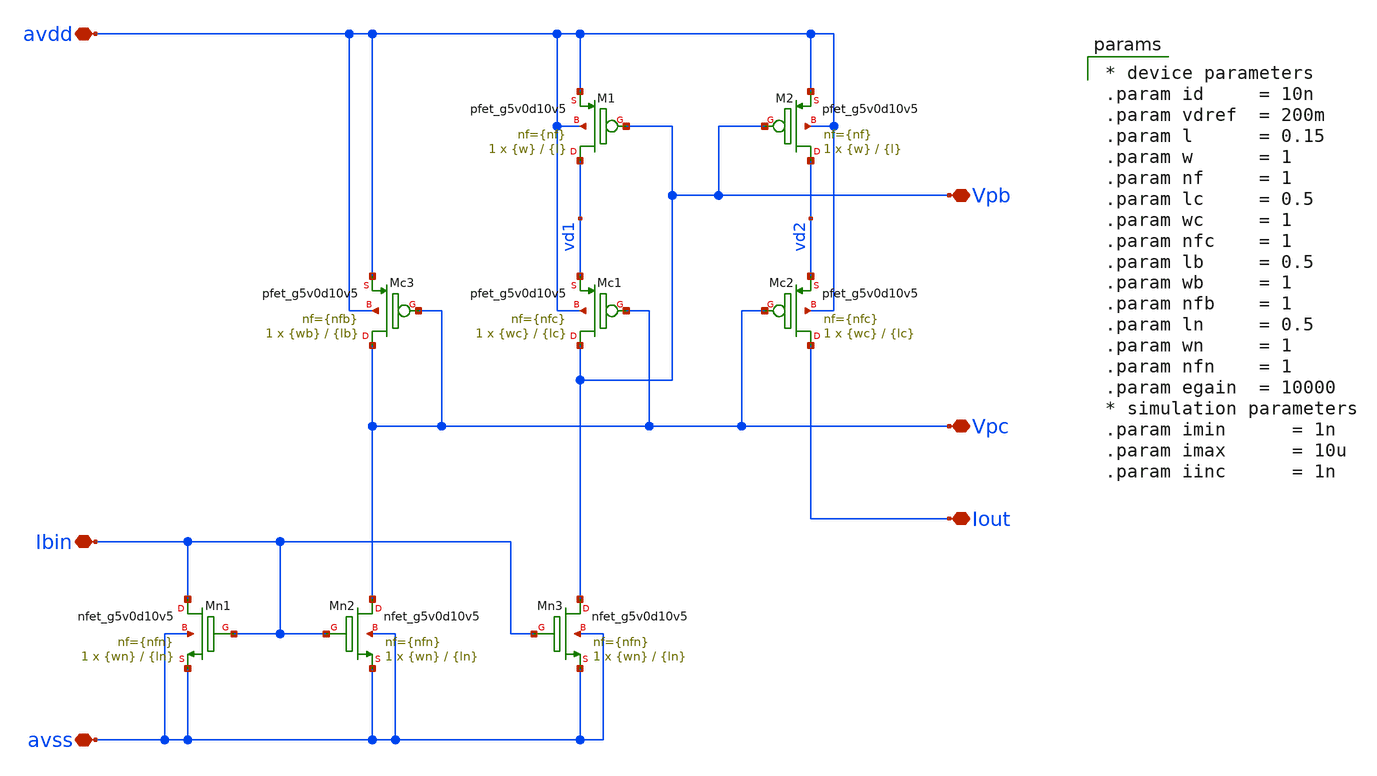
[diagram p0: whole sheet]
** sch_path: xschem/sky130_cm_ip__biasgen.sch
**.subckt sky130_cm_ip__biasgen avss avdd Ibin Vpb Vpc Iout
*.iopin avss
*.iopin avdd
*.iopin Ibin
*.iopin Vpb
*.iopin Vpc
*.iopin Iout
XMc1 Vpb Vpc vd1 avdd sky130_fd_pr__pfet_g5v0d10v5 L={lc} W={wc} nf={nfc} ad='int(({nfc} + 1)/2) * {wc} / {nfc} * 0.29'
+ as='int(({nfc} + 2)/2) * {wc} / {nfc} * 0.29' pd='2*int(({nfc} + 1)/2) * ({wc} / {nfc} + 0.29)' ps='2*int(({nfc} + 2)/2) * ({wc} / {nfc} + 0.29)'
+ nrd='0.29 / {wc} ' nrs='0.29 / {wc} ' sa=0 sb=0 sd=0 mult=1 m=1
XM1 vd1 Vpb avdd avdd sky130_fd_pr__pfet_g5v0d10v5 L={l} W={w} nf={nf} ad='int(({nf} + 1)/2) * {w} / {nf} * 0.29'
+ as='int(({nf} + 2)/2) * {w} / {nf} * 0.29' pd='2*int(({nf} + 1)/2) * ({w} / {nf} + 0.29)' ps='2*int(({nf} + 2)/2) * ({w} / {nf} + 0.29)'
+ nrd='0.29 / {w} ' nrs='0.29 / {w} ' sa=0 sb=0 sd=0 mult=1 m=1
XMc2 Iout Vpc vd2 avdd sky130_fd_pr__pfet_g5v0d10v5 L={lc} W={wc} nf={nfc} ad='int(({nfc} + 1)/2) * {wc} / {nfc} * 0.29'
+ as='int(({nfc} + 2)/2) * {wc} / {nfc} * 0.29' pd='2*int(({nfc} + 1)/2) * ({wc} / {nfc} + 0.29)' ps='2*int(({nfc} + 2)/2) * ({wc} / {nfc} + 0.29)'
+ nrd='0.29 / {wc} ' nrs='0.29 / {wc} ' sa=0 sb=0 sd=0 mult=1 m=1
XM2 vd2 Vpb avdd avdd sky130_fd_pr__pfet_g5v0d10v5 L={l} W={w} nf={nf} ad='int(({nf} + 1)/2) * {w} / {nf} * 0.29'
+ as='int(({nf} + 2)/2) * {w} / {nf} * 0.29' pd='2*int(({nf} + 1)/2) * ({w} / {nf} + 0.29)' ps='2*int(({nf} + 2)/2) * ({w} / {nf} + 0.29)'
+ nrd='0.29 / {w} ' nrs='0.29 / {w} ' sa=0 sb=0 sd=0 mult=1 m=1
XMc3 Vpc Vpc avdd avdd sky130_fd_pr__pfet_g5v0d10v5 L={lb} W={wb} nf={nfb} ad='int(({nfb} + 1)/2) * {wb} / {nfb} * 0.29'
+ as='int(({nfb} + 2)/2) * {wb} / {nfb} * 0.29' pd='2*int(({nfb} + 1)/2) * ({wb} / {nfb} + 0.29)' ps='2*int(({nfb} + 2)/2) * ({wb} / {nfb} + 0.29)'
+ nrd='0.29 / {wb} ' nrs='0.29 / {wb} ' sa=0 sb=0 sd=0 mult=1 m=1
XMn1 Ibin Ibin avss avss sky130_fd_pr__nfet_g5v0d10v5 L={ln} W={wn} nf={nfn} ad='int(({nfn} + 1)/2) * {wn} / {nfn} * 0.29'
+ as='int(({nfn} + 2)/2) * {wn} / {nfn} * 0.29' pd='2*int(({nfn} + 1)/2) * ({wn} / {nfn} + 0.29)' ps='2*int(({nfn} + 2)/2) * ({wn} / {nfn} + 0.29)'
+ nrd='0.29 / {wn} ' nrs='0.29 / {wn} ' sa=0 sb=0 sd=0 mult=1 m=1
XMn2 Vpc Ibin avss avss sky130_fd_pr__nfet_g5v0d10v5 L={ln} W={wn} nf={nfn} ad='int(({nfn} + 1)/2) * {wn} / {nfn} * 0.29'
+ as='int(({nfn} + 2)/2) * {wn} / {nfn} * 0.29' pd='2*int(({nfn} + 1)/2) * ({wn} / {nfn} + 0.29)' ps='2*int(({nfn} + 2)/2) * ({wn} / {nfn} + 0.29)'
+ nrd='0.29 / {wn} ' nrs='0.29 / {wn} ' sa=0 sb=0 sd=0 mult=1 m=1
XMn3 Vpb Ibin avss avss sky130_fd_pr__nfet_g5v0d10v5 L={ln} W={wn} nf={nfn} ad='int(({nfn} + 1)/2) * {wn} / {nfn} * 0.29'
+ as='int(({nfn} + 2)/2) * {wn} / {nfn} * 0.29' pd='2*int(({nfn} + 1)/2) * ({wn} / {nfn} + 0.29)' ps='2*int(({nfn} + 2)/2) * ({wn} / {nfn} + 0.29)'
+ nrd='0.29 / {wn} ' nrs='0.29 / {wn} ' sa=0 sb=0 sd=0 mult=1 m=1
**** begin user architecture code

* device parameters
.param id     = 10n
.param vdref  = 200m
.param l      = 0.15
.param w      = 1
.param nf     = 1
.param lc     = 0.5
.param wc     = 1
.param nfc    = 1
.param lb     = 0.5
.param wb     = 1
.param nfb    = 1
.param ln     = 0.5
.param wn     = 1
.param nfn    = 1
.param egain  = 10000
* simulation parameters
.param imin      = 1n
.param imax      = 10u
.param iinc      = 1n


**** end user architecture code
**.ends
.end
